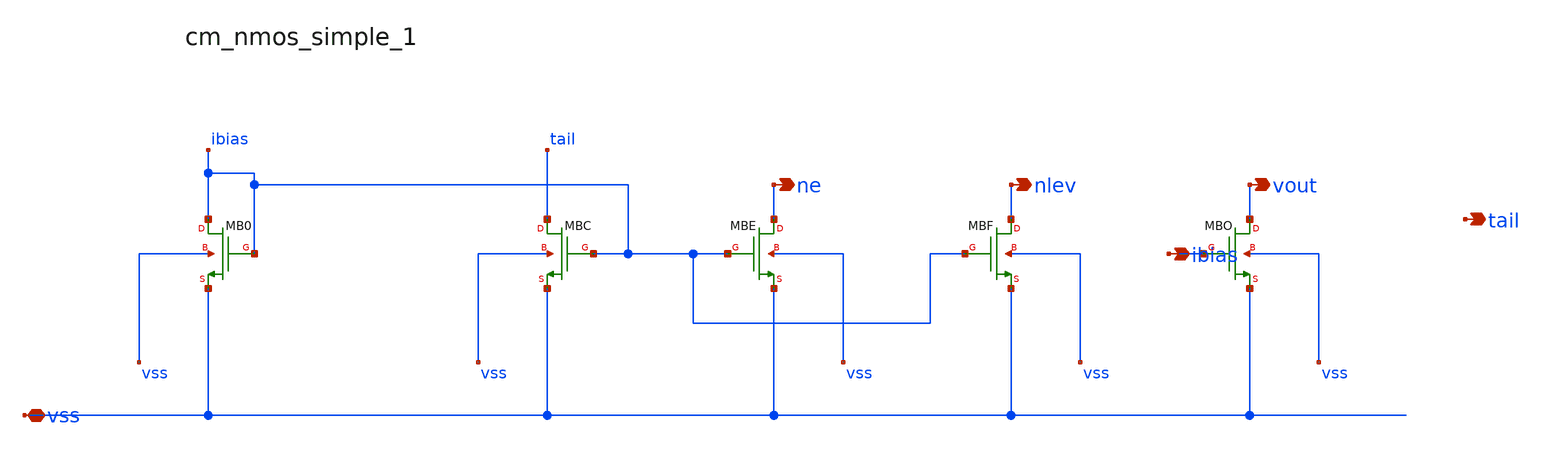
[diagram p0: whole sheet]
** sch_path: analog-db/raw/amp_019_ti_ldo_error/hier/blocks/cm_nmos_simple_1.sch
**.subckt cm_nmos_simple_1 vss ibias ne nlev vout tail
*.iopin vss
*.opin ibias
*.opin ne
*.opin nlev
*.opin vout
*.opin tail
XMB0 ibias ibias vss vss sg13_hv_nmos w=x_dut_xmb0_w l=x_dut_xmb0_l ng=1 m=1
XMBC tail ibias vss vss sg13_hv_nmos w=x_dut_xmbc_w l=x_dut_xmbc_l ng=1 m=x_dut_xmbc_m
XMBE ne ibias vss vss sg13_hv_nmos w=x_dut_xmbe_w l=x_dut_xmbe_l ng=1 m=1
XMBF nlev ibias vss vss sg13_hv_nmos w=x_dut_xmbf_w l=x_dut_xmbf_l ng=1 m=1
XMBO vout ibias vss vss sg13_hv_nmos w=x_dut_xmbo_w l=x_dut_xmbo_l ng=1 m=x_dut_xmbo_m
**.ends
.end
